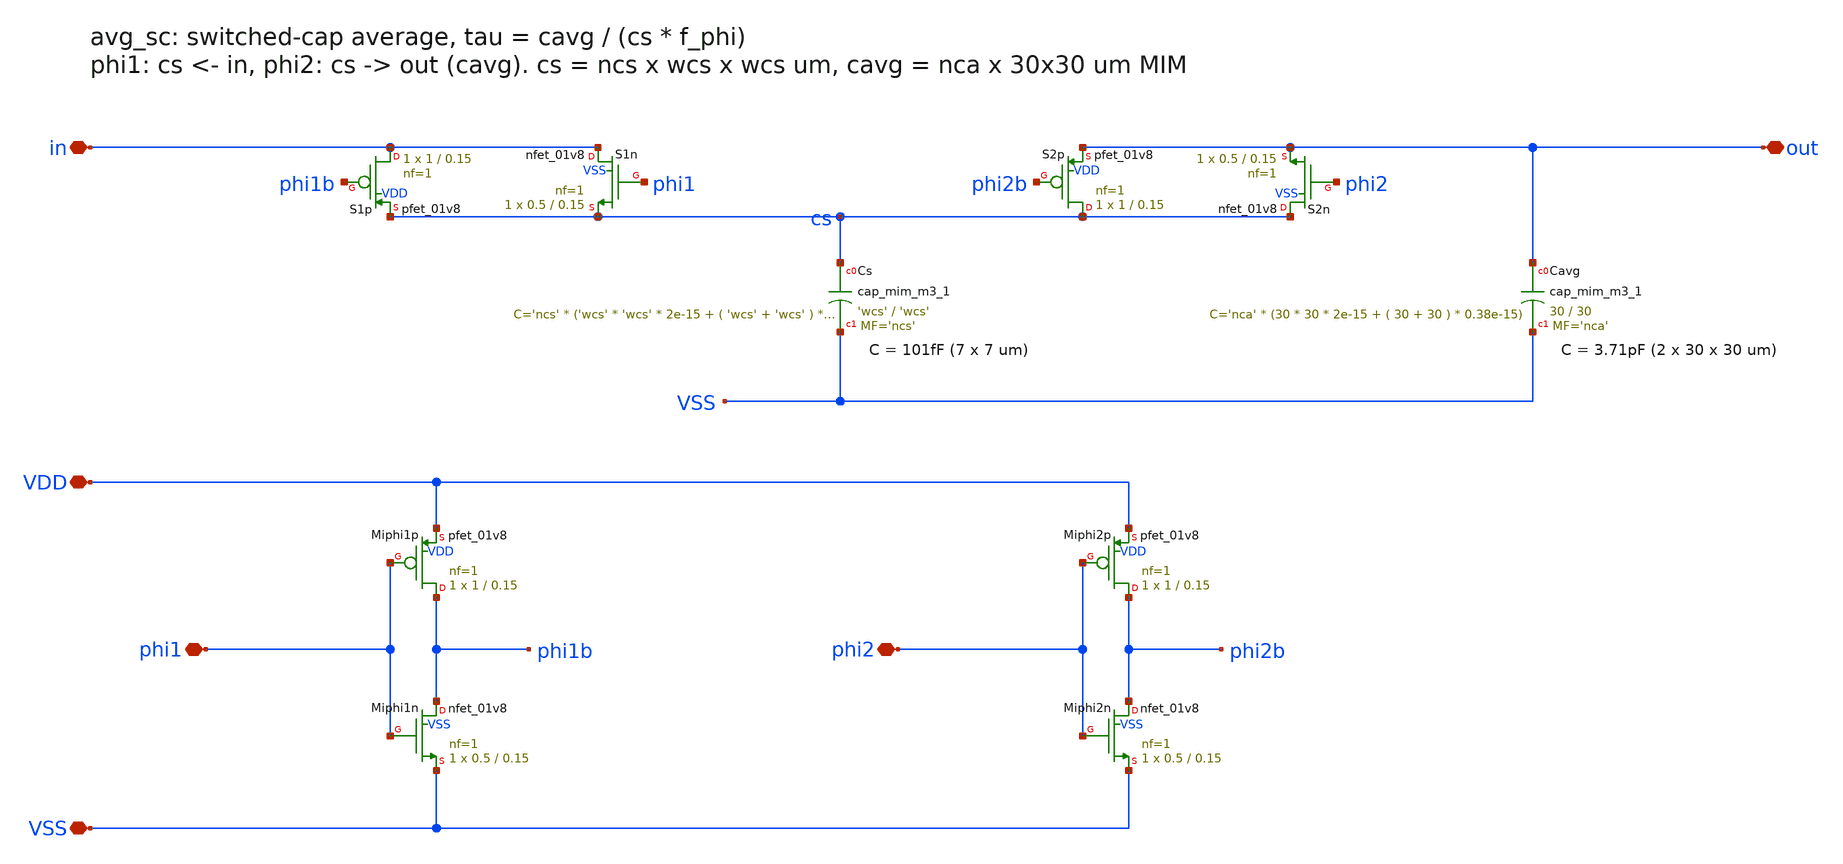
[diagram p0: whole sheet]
** sch_path: xschem/avg_sc.sch
**.subckt avg_sc VDD VSS in out phi1 phi2
*.iopin VDD
*.iopin VSS
*.iopin in
*.iopin out
*.iopin phi1
*.iopin phi2
XMiphi1p phi1b phi1 VDD VDD sky130_fd_pr__pfet_01v8 L=0.15 W=1 nf=1 ad='int((nf+1)/2) * W/nf * 0.29'
+ as='int((nf+2)/2) * W/nf * 0.29' pd='2*int((nf+1)/2) * (W/nf + 0.29)' ps='2*int((nf+2)/2) * (W/nf + 0.29)'
+ nrd='0.29 / W' nrs='0.29 / W' sa=0 sb=0 sd=0 mult=1 m=1
XMiphi1n phi1b phi1 VSS VSS sky130_fd_pr__nfet_01v8 L=0.15 W=0.5 nf=1 ad='int((nf+1)/2) * W/nf * 0.29'
+ as='int((nf+2)/2) * W/nf * 0.29' pd='2*int((nf+1)/2) * (W/nf + 0.29)' ps='2*int((nf+2)/2) * (W/nf + 0.29)'
+ nrd='0.29 / W' nrs='0.29 / W' sa=0 sb=0 sd=0 mult=1 m=1
XMiphi2p phi2b phi2 VDD VDD sky130_fd_pr__pfet_01v8 L=0.15 W=1 nf=1 ad='int((nf+1)/2) * W/nf * 0.29'
+ as='int((nf+2)/2) * W/nf * 0.29' pd='2*int((nf+1)/2) * (W/nf + 0.29)' ps='2*int((nf+2)/2) * (W/nf + 0.29)'
+ nrd='0.29 / W' nrs='0.29 / W' sa=0 sb=0 sd=0 mult=1 m=1
XMiphi2n phi2b phi2 VSS VSS sky130_fd_pr__nfet_01v8 L=0.15 W=0.5 nf=1 ad='int((nf+1)/2) * W/nf * 0.29'
+ as='int((nf+2)/2) * W/nf * 0.29' pd='2*int((nf+1)/2) * (W/nf + 0.29)' ps='2*int((nf+2)/2) * (W/nf + 0.29)'
+ nrd='0.29 / W' nrs='0.29 / W' sa=0 sb=0 sd=0 mult=1 m=1
XS1n in phi1 cs VSS sky130_fd_pr__nfet_01v8 L=0.15 W=0.5 nf=1 ad='int((nf+1)/2) * W/nf * 0.29' as='int((nf+2)/2) * W/nf * 0.29'
+ pd='2*int((nf+1)/2) * (W/nf + 0.29)' ps='2*int((nf+2)/2) * (W/nf + 0.29)' nrd='0.29 / W' nrs='0.29 / W'
+ sa=0 sb=0 sd=0 mult=1 m=1
XS1p in phi1b cs VDD sky130_fd_pr__pfet_01v8 L=0.15 W=1 nf=1 ad='int((nf+1)/2) * W/nf * 0.29' as='int((nf+2)/2) * W/nf * 0.29'
+ pd='2*int((nf+1)/2) * (W/nf + 0.29)' ps='2*int((nf+2)/2) * (W/nf + 0.29)' nrd='0.29 / W' nrs='0.29 / W'
+ sa=0 sb=0 sd=0 mult=1 m=1
XS2n cs phi2 out VSS sky130_fd_pr__nfet_01v8 L=0.15 W=0.5 nf=1 ad='int((nf+1)/2) * W/nf * 0.29' as='int((nf+2)/2) * W/nf * 0.29'
+ pd='2*int((nf+1)/2) * (W/nf + 0.29)' ps='2*int((nf+2)/2) * (W/nf + 0.29)' nrd='0.29 / W' nrs='0.29 / W'
+ sa=0 sb=0 sd=0 mult=1 m=1
XS2p cs phi2b out VDD sky130_fd_pr__pfet_01v8 L=0.15 W=1 nf=1 ad='int((nf+1)/2) * W/nf * 0.29' as='int((nf+2)/2) * W/nf * 0.29'
+ pd='2*int((nf+1)/2) * (W/nf + 0.29)' ps='2*int((nf+2)/2) * (W/nf + 0.29)' nrd='0.29 / W' nrs='0.29 / W'
+ sa=0 sb=0 sd=0 mult=1 m=1
XCs cs VSS sky130_fd_pr__cap_mim_m3_1 W='wcs' L='wcs' MF='ncs' m='ncs'
XCavg out VSS sky130_fd_pr__cap_mim_m3_1 W=30 L=30 MF='nca' m='nca'
**.ends
.end
